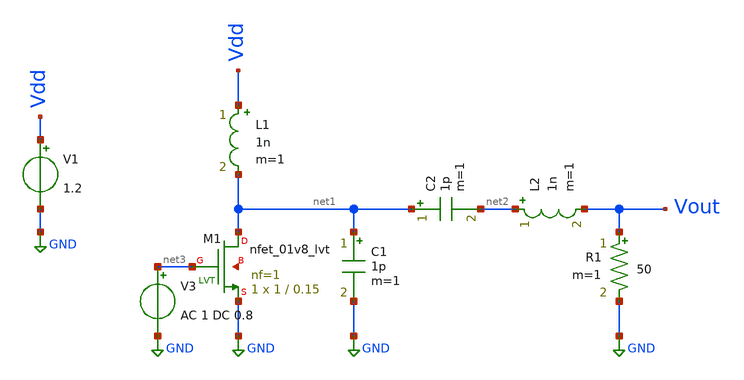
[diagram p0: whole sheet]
** sch_path: skywater_stuff/ECE631_RF_CMOS/untitled-4.sch
**.subckt untitled-4
XM1 net1 net3 GND net4 sky130_fd_pr__nfet_01v8_lvt L=0.15 W=1 nf=1 ad='int((nf+1)/2) * W/nf * 0.29' as='int((nf+2)/2) * W/nf * 0.29'
+ pd='2*int((nf+1)/2) * (W/nf + 0.29)' ps='2*int((nf+2)/2) * (W/nf + 0.29)' nrd='0.29 / W' nrs='0.29 / W'
+ sa=0 sb=0 sd=0 mult=1 m=1
L1 Vdd net1 1n m=1
C1 net1 GND 1p m=1
C2 net1 net2 1p m=1
L2 net2 Vout 1n m=1
R1 Vout GND 50 m=1
V1 Vdd GND 1.2
V3 net3 GND AC 1 DC 0.8
**.ends
.GLOBAL GND
.end
